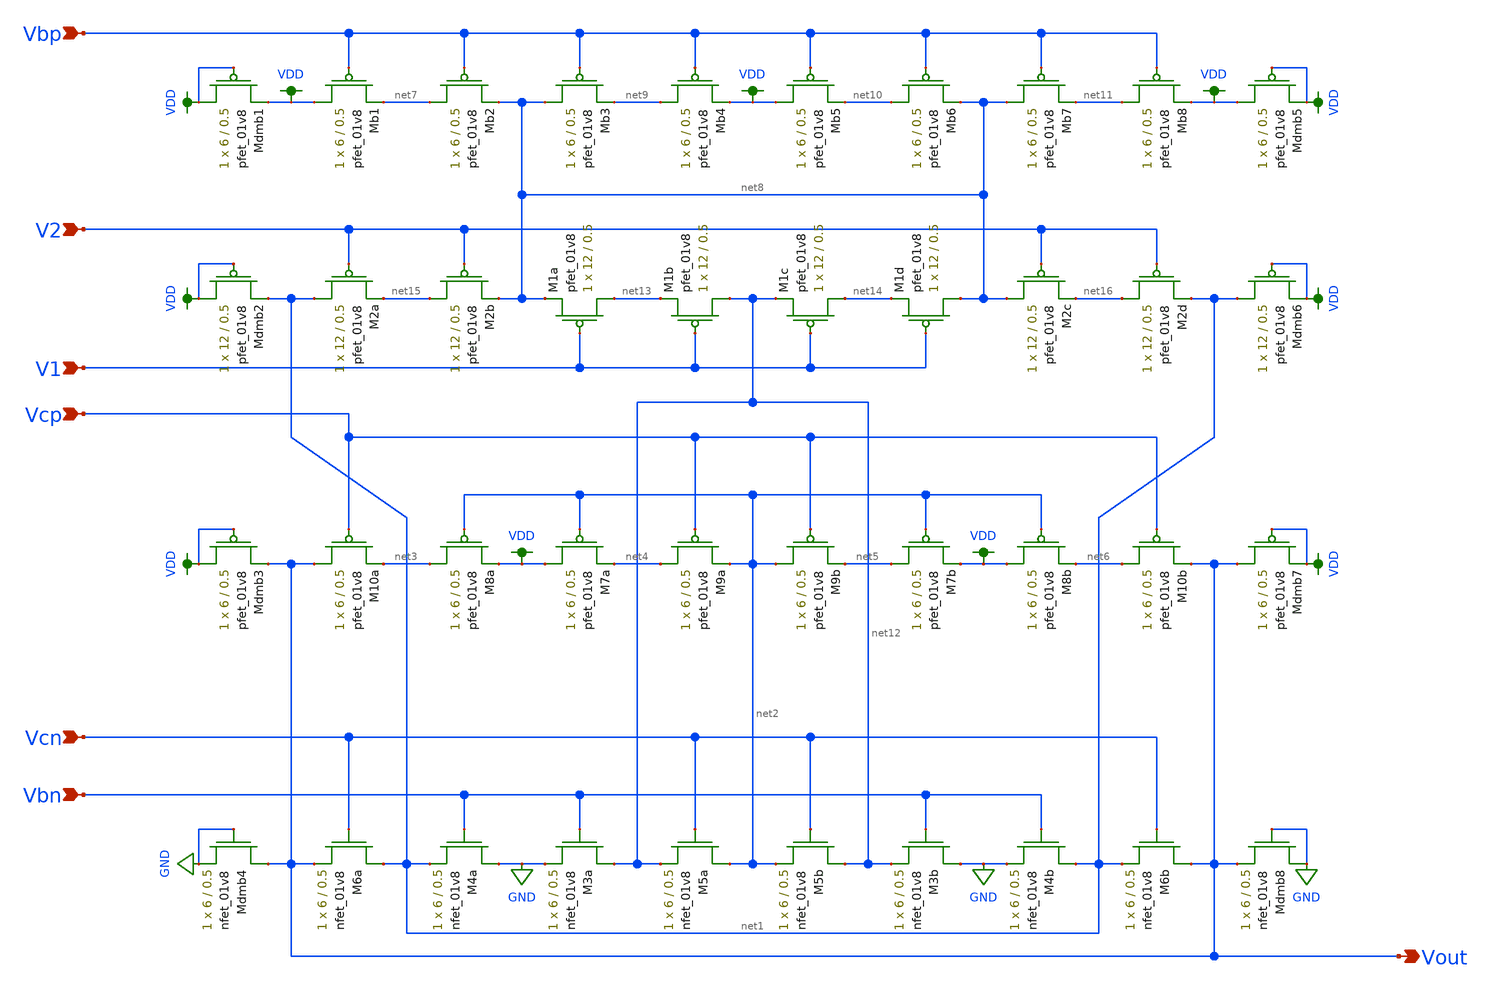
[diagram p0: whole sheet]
** sch_path: mini3/schem/cas_diff_lvs.sch
**.subckt cas_diff_lvs Vbp Vbn Vcn Vcp Vout V1 V2
*.ipin Vbp
*.ipin Vbn
*.ipin Vcn
*.ipin Vcp
*.opin Vout
*.ipin V1
*.ipin V2
XM6a net1 Vcn Vout GND sky130_fd_pr__nfet_01v8 L=0.5 W=6 nf=1 ad='int((nf+1)/2) * W/nf * 0.29' as='int((nf+2)/2) * W/nf * 0.29'
+ pd='2*int((nf+1)/2) * (W/nf + 0.29)' ps='2*int((nf+2)/2) * (W/nf + 0.29)' nrd='0.29 / W' nrs='0.29 / W'
+ sa=0 sb=0 sd=0 mult=1 m=1
XM4a GND Vbn net1 GND sky130_fd_pr__nfet_01v8 L=0.5 W=6 nf=1 ad='int((nf+1)/2) * W/nf * 0.29' as='int((nf+2)/2) * W/nf * 0.29'
+ pd='2*int((nf+1)/2) * (W/nf + 0.29)' ps='2*int((nf+2)/2) * (W/nf + 0.29)' nrd='0.29 / W' nrs='0.29 / W'
+ sa=0 sb=0 sd=0 mult=1 m=1
XM3a net12 Vbn GND GND sky130_fd_pr__nfet_01v8 L=0.5 W=6 nf=1 ad='int((nf+1)/2) * W/nf * 0.29' as='int((nf+2)/2) * W/nf * 0.29'
+ pd='2*int((nf+1)/2) * (W/nf + 0.29)' ps='2*int((nf+2)/2) * (W/nf + 0.29)' nrd='0.29 / W' nrs='0.29 / W'
+ sa=0 sb=0 sd=0 mult=1 m=1
XM5a net2 Vcn net12 GND sky130_fd_pr__nfet_01v8 L=0.5 W=6 nf=1 ad='int((nf+1)/2) * W/nf * 0.29' as='int((nf+2)/2) * W/nf * 0.29'
+ pd='2*int((nf+1)/2) * (W/nf + 0.29)' ps='2*int((nf+2)/2) * (W/nf + 0.29)' nrd='0.29 / W' nrs='0.29 / W'
+ sa=0 sb=0 sd=0 mult=1 m=1
XM5b net12 Vcn net2 GND sky130_fd_pr__nfet_01v8 L=0.5 W=6 nf=1 ad='int((nf+1)/2) * W/nf * 0.29' as='int((nf+2)/2) * W/nf * 0.29'
+ pd='2*int((nf+1)/2) * (W/nf + 0.29)' ps='2*int((nf+2)/2) * (W/nf + 0.29)' nrd='0.29 / W' nrs='0.29 / W'
+ sa=0 sb=0 sd=0 mult=1 m=1
XM3b GND Vbn net12 GND sky130_fd_pr__nfet_01v8 L=0.5 W=6 nf=1 ad='int((nf+1)/2) * W/nf * 0.29' as='int((nf+2)/2) * W/nf * 0.29'
+ pd='2*int((nf+1)/2) * (W/nf + 0.29)' ps='2*int((nf+2)/2) * (W/nf + 0.29)' nrd='0.29 / W' nrs='0.29 / W'
+ sa=0 sb=0 sd=0 mult=1 m=1
XM4b net1 Vbn GND GND sky130_fd_pr__nfet_01v8 L=0.5 W=6 nf=1 ad='int((nf+1)/2) * W/nf * 0.29' as='int((nf+2)/2) * W/nf * 0.29'
+ pd='2*int((nf+1)/2) * (W/nf + 0.29)' ps='2*int((nf+2)/2) * (W/nf + 0.29)' nrd='0.29 / W' nrs='0.29 / W'
+ sa=0 sb=0 sd=0 mult=1 m=1
XM6b Vout Vcn net1 GND sky130_fd_pr__nfet_01v8 L=0.5 W=6 nf=1 ad='int((nf+1)/2) * W/nf * 0.29' as='int((nf+2)/2) * W/nf * 0.29'
+ pd='2*int((nf+1)/2) * (W/nf + 0.29)' ps='2*int((nf+2)/2) * (W/nf + 0.29)' nrd='0.29 / W' nrs='0.29 / W'
+ sa=0 sb=0 sd=0 mult=1 m=1
XM10a Vout Vcp net3 VDD sky130_fd_pr__pfet_01v8 L=0.5 W=6 nf=1 ad='int((nf+1)/2) * W/nf * 0.29' as='int((nf+2)/2) * W/nf * 0.29'
+ pd='2*int((nf+1)/2) * (W/nf + 0.29)' ps='2*int((nf+2)/2) * (W/nf + 0.29)' nrd='0.29 / W' nrs='0.29 / W'
+ sa=0 sb=0 sd=0 mult=1 m=1
XM8a net3 net2 VDD VDD sky130_fd_pr__pfet_01v8 L=0.5 W=6 nf=1 ad='int((nf+1)/2) * W/nf * 0.29' as='int((nf+2)/2) * W/nf * 0.29'
+ pd='2*int((nf+1)/2) * (W/nf + 0.29)' ps='2*int((nf+2)/2) * (W/nf + 0.29)' nrd='0.29 / W' nrs='0.29 / W'
+ sa=0 sb=0 sd=0 mult=1 m=1
XM7a VDD net2 net4 VDD sky130_fd_pr__pfet_01v8 L=0.5 W=6 nf=1 ad='int((nf+1)/2) * W/nf * 0.29' as='int((nf+2)/2) * W/nf * 0.29'
+ pd='2*int((nf+1)/2) * (W/nf + 0.29)' ps='2*int((nf+2)/2) * (W/nf + 0.29)' nrd='0.29 / W' nrs='0.29 / W'
+ sa=0 sb=0 sd=0 mult=1 m=1
XM9a net4 Vcp net2 VDD sky130_fd_pr__pfet_01v8 L=0.5 W=6 nf=1 ad='int((nf+1)/2) * W/nf * 0.29' as='int((nf+2)/2) * W/nf * 0.29'
+ pd='2*int((nf+1)/2) * (W/nf + 0.29)' ps='2*int((nf+2)/2) * (W/nf + 0.29)' nrd='0.29 / W' nrs='0.29 / W'
+ sa=0 sb=0 sd=0 mult=1 m=1
XM9b net2 Vcp net5 VDD sky130_fd_pr__pfet_01v8 L=0.5 W=6 nf=1 ad='int((nf+1)/2) * W/nf * 0.29' as='int((nf+2)/2) * W/nf * 0.29'
+ pd='2*int((nf+1)/2) * (W/nf + 0.29)' ps='2*int((nf+2)/2) * (W/nf + 0.29)' nrd='0.29 / W' nrs='0.29 / W'
+ sa=0 sb=0 sd=0 mult=1 m=1
XM7b net5 net2 VDD VDD sky130_fd_pr__pfet_01v8 L=0.5 W=6 nf=1 ad='int((nf+1)/2) * W/nf * 0.29' as='int((nf+2)/2) * W/nf * 0.29'
+ pd='2*int((nf+1)/2) * (W/nf + 0.29)' ps='2*int((nf+2)/2) * (W/nf + 0.29)' nrd='0.29 / W' nrs='0.29 / W'
+ sa=0 sb=0 sd=0 mult=1 m=1
XM8b VDD net2 net6 VDD sky130_fd_pr__pfet_01v8 L=0.5 W=6 nf=1 ad='int((nf+1)/2) * W/nf * 0.29' as='int((nf+2)/2) * W/nf * 0.29'
+ pd='2*int((nf+1)/2) * (W/nf + 0.29)' ps='2*int((nf+2)/2) * (W/nf + 0.29)' nrd='0.29 / W' nrs='0.29 / W'
+ sa=0 sb=0 sd=0 mult=1 m=1
XM10b net6 Vcp Vout VDD sky130_fd_pr__pfet_01v8 L=0.5 W=6 nf=1 ad='int((nf+1)/2) * W/nf * 0.29' as='int((nf+2)/2) * W/nf * 0.29'
+ pd='2*int((nf+1)/2) * (W/nf + 0.29)' ps='2*int((nf+2)/2) * (W/nf + 0.29)' nrd='0.29 / W' nrs='0.29 / W'
+ sa=0 sb=0 sd=0 mult=1 m=1
XMb1 VDD Vbp net7 VDD sky130_fd_pr__pfet_01v8 L=0.5 W=6 nf=1 ad='int((nf+1)/2) * W/nf * 0.29' as='int((nf+2)/2) * W/nf * 0.29'
+ pd='2*int((nf+1)/2) * (W/nf + 0.29)' ps='2*int((nf+2)/2) * (W/nf + 0.29)' nrd='0.29 / W' nrs='0.29 / W'
+ sa=0 sb=0 sd=0 mult=1 m=1
XMb2 net7 Vbp net8 VDD sky130_fd_pr__pfet_01v8 L=0.5 W=6 nf=1 ad='int((nf+1)/2) * W/nf * 0.29' as='int((nf+2)/2) * W/nf * 0.29'
+ pd='2*int((nf+1)/2) * (W/nf + 0.29)' ps='2*int((nf+2)/2) * (W/nf + 0.29)' nrd='0.29 / W' nrs='0.29 / W'
+ sa=0 sb=0 sd=0 mult=1 m=1
XMb3 net8 Vbp net9 VDD sky130_fd_pr__pfet_01v8 L=0.5 W=6 nf=1 ad='int((nf+1)/2) * W/nf * 0.29' as='int((nf+2)/2) * W/nf * 0.29'
+ pd='2*int((nf+1)/2) * (W/nf + 0.29)' ps='2*int((nf+2)/2) * (W/nf + 0.29)' nrd='0.29 / W' nrs='0.29 / W'
+ sa=0 sb=0 sd=0 mult=1 m=1
XMb4 net9 Vbp VDD VDD sky130_fd_pr__pfet_01v8 L=0.5 W=6 nf=1 ad='int((nf+1)/2) * W/nf * 0.29' as='int((nf+2)/2) * W/nf * 0.29'
+ pd='2*int((nf+1)/2) * (W/nf + 0.29)' ps='2*int((nf+2)/2) * (W/nf + 0.29)' nrd='0.29 / W' nrs='0.29 / W'
+ sa=0 sb=0 sd=0 mult=1 m=1
XMb5 VDD Vbp net10 VDD sky130_fd_pr__pfet_01v8 L=0.5 W=6 nf=1 ad='int((nf+1)/2) * W/nf * 0.29' as='int((nf+2)/2) * W/nf * 0.29'
+ pd='2*int((nf+1)/2) * (W/nf + 0.29)' ps='2*int((nf+2)/2) * (W/nf + 0.29)' nrd='0.29 / W' nrs='0.29 / W'
+ sa=0 sb=0 sd=0 mult=1 m=1
XMb6 net10 Vbp net8 VDD sky130_fd_pr__pfet_01v8 L=0.5 W=6 nf=1 ad='int((nf+1)/2) * W/nf * 0.29' as='int((nf+2)/2) * W/nf * 0.29'
+ pd='2*int((nf+1)/2) * (W/nf + 0.29)' ps='2*int((nf+2)/2) * (W/nf + 0.29)' nrd='0.29 / W' nrs='0.29 / W'
+ sa=0 sb=0 sd=0 mult=1 m=1
XMb7 net8 Vbp net11 VDD sky130_fd_pr__pfet_01v8 L=0.5 W=6 nf=1 ad='int((nf+1)/2) * W/nf * 0.29' as='int((nf+2)/2) * W/nf * 0.29'
+ pd='2*int((nf+1)/2) * (W/nf + 0.29)' ps='2*int((nf+2)/2) * (W/nf + 0.29)' nrd='0.29 / W' nrs='0.29 / W'
+ sa=0 sb=0 sd=0 mult=1 m=1
XMb8 net11 Vbp VDD VDD sky130_fd_pr__pfet_01v8 L=0.5 W=6 nf=1 ad='int((nf+1)/2) * W/nf * 0.29' as='int((nf+2)/2) * W/nf * 0.29'
+ pd='2*int((nf+1)/2) * (W/nf + 0.29)' ps='2*int((nf+2)/2) * (W/nf + 0.29)' nrd='0.29 / W' nrs='0.29 / W'
+ sa=0 sb=0 sd=0 mult=1 m=1
XM1a net13 V1 net8 VDD sky130_fd_pr__pfet_01v8 L=0.5 W=12 nf=1 ad='int((nf+1)/2) * W/nf * 0.29' as='int((nf+2)/2) * W/nf * 0.29'
+ pd='2*int((nf+1)/2) * (W/nf + 0.29)' ps='2*int((nf+2)/2) * (W/nf + 0.29)' nrd='0.29 / W' nrs='0.29 / W'
+ sa=0 sb=0 sd=0 mult=1 m=1
XM1b net12 V1 net13 VDD sky130_fd_pr__pfet_01v8 L=0.5 W=12 nf=1 ad='int((nf+1)/2) * W/nf * 0.29' as='int((nf+2)/2) * W/nf * 0.29'
+ pd='2*int((nf+1)/2) * (W/nf + 0.29)' ps='2*int((nf+2)/2) * (W/nf + 0.29)' nrd='0.29 / W' nrs='0.29 / W'
+ sa=0 sb=0 sd=0 mult=1 m=1
XM2a net1 V2 net15 VDD sky130_fd_pr__pfet_01v8 L=0.5 W=12 nf=1 ad='int((nf+1)/2) * W/nf * 0.29' as='int((nf+2)/2) * W/nf * 0.29'
+ pd='2*int((nf+1)/2) * (W/nf + 0.29)' ps='2*int((nf+2)/2) * (W/nf + 0.29)' nrd='0.29 / W' nrs='0.29 / W'
+ sa=0 sb=0 sd=0 mult=1 m=1
XM2b net15 V2 net8 VDD sky130_fd_pr__pfet_01v8 L=0.5 W=12 nf=1 ad='int((nf+1)/2) * W/nf * 0.29' as='int((nf+2)/2) * W/nf * 0.29'
+ pd='2*int((nf+1)/2) * (W/nf + 0.29)' ps='2*int((nf+2)/2) * (W/nf + 0.29)' nrd='0.29 / W' nrs='0.29 / W'
+ sa=0 sb=0 sd=0 mult=1 m=1
XM2c net8 V2 net16 VDD sky130_fd_pr__pfet_01v8 L=0.5 W=12 nf=1 ad='int((nf+1)/2) * W/nf * 0.29' as='int((nf+2)/2) * W/nf * 0.29'
+ pd='2*int((nf+1)/2) * (W/nf + 0.29)' ps='2*int((nf+2)/2) * (W/nf + 0.29)' nrd='0.29 / W' nrs='0.29 / W'
+ sa=0 sb=0 sd=0 mult=1 m=1
XM2d net16 V2 net1 VDD sky130_fd_pr__pfet_01v8 L=0.5 W=12 nf=1 ad='int((nf+1)/2) * W/nf * 0.29' as='int((nf+2)/2) * W/nf * 0.29'
+ pd='2*int((nf+1)/2) * (W/nf + 0.29)' ps='2*int((nf+2)/2) * (W/nf + 0.29)' nrd='0.29 / W' nrs='0.29 / W'
+ sa=0 sb=0 sd=0 mult=1 m=1
XM1c net14 V1 net12 VDD sky130_fd_pr__pfet_01v8 L=0.5 W=12 nf=1 ad='int((nf+1)/2) * W/nf * 0.29' as='int((nf+2)/2) * W/nf * 0.29'
+ pd='2*int((nf+1)/2) * (W/nf + 0.29)' ps='2*int((nf+2)/2) * (W/nf + 0.29)' nrd='0.29 / W' nrs='0.29 / W'
+ sa=0 sb=0 sd=0 mult=1 m=1
XM1d net8 V1 net14 VDD sky130_fd_pr__pfet_01v8 L=0.5 W=12 nf=1 ad='int((nf+1)/2) * W/nf * 0.29' as='int((nf+2)/2) * W/nf * 0.29'
+ pd='2*int((nf+1)/2) * (W/nf + 0.29)' ps='2*int((nf+2)/2) * (W/nf + 0.29)' nrd='0.29 / W' nrs='0.29 / W'
+ sa=0 sb=0 sd=0 mult=1 m=1
XMdmb3 VDD VDD Vout VDD sky130_fd_pr__pfet_01v8 L=0.5 W=6 nf=1 ad='int((nf+1)/2) * W/nf * 0.29' as='int((nf+2)/2) * W/nf * 0.29'
+ pd='2*int((nf+1)/2) * (W/nf + 0.29)' ps='2*int((nf+2)/2) * (W/nf + 0.29)' nrd='0.29 / W' nrs='0.29 / W'
+ sa=0 sb=0 sd=0 mult=1 m=1
XMdmb2 VDD VDD net1 VDD sky130_fd_pr__pfet_01v8 L=0.5 W=12 nf=1 ad='int((nf+1)/2) * W/nf * 0.29' as='int((nf+2)/2) * W/nf * 0.29'
+ pd='2*int((nf+1)/2) * (W/nf + 0.29)' ps='2*int((nf+2)/2) * (W/nf + 0.29)' nrd='0.29 / W' nrs='0.29 / W'
+ sa=0 sb=0 sd=0 mult=1 m=1
XMdmb1 VDD VDD VDD VDD sky130_fd_pr__pfet_01v8 L=0.5 W=6 nf=1 ad='int((nf+1)/2) * W/nf * 0.29' as='int((nf+2)/2) * W/nf * 0.29'
+ pd='2*int((nf+1)/2) * (W/nf + 0.29)' ps='2*int((nf+2)/2) * (W/nf + 0.29)' nrd='0.29 / W' nrs='0.29 / W'
+ sa=0 sb=0 sd=0 mult=1 m=1
XMdmb7 Vout VDD VDD VDD sky130_fd_pr__pfet_01v8 L=0.5 W=6 nf=1 ad='int((nf+1)/2) * W/nf * 0.29' as='int((nf+2)/2) * W/nf * 0.29'
+ pd='2*int((nf+1)/2) * (W/nf + 0.29)' ps='2*int((nf+2)/2) * (W/nf + 0.29)' nrd='0.29 / W' nrs='0.29 / W'
+ sa=0 sb=0 sd=0 mult=1 m=1
XMdmb6 net1 VDD VDD VDD sky130_fd_pr__pfet_01v8 L=0.5 W=12 nf=1 ad='int((nf+1)/2) * W/nf * 0.29' as='int((nf+2)/2) * W/nf * 0.29'
+ pd='2*int((nf+1)/2) * (W/nf + 0.29)' ps='2*int((nf+2)/2) * (W/nf + 0.29)' nrd='0.29 / W' nrs='0.29 / W'
+ sa=0 sb=0 sd=0 mult=1 m=1
XMdmb5 VDD VDD VDD VDD sky130_fd_pr__pfet_01v8 L=0.5 W=6 nf=1 ad='int((nf+1)/2) * W/nf * 0.29' as='int((nf+2)/2) * W/nf * 0.29'
+ pd='2*int((nf+1)/2) * (W/nf + 0.29)' ps='2*int((nf+2)/2) * (W/nf + 0.29)' nrd='0.29 / W' nrs='0.29 / W'
+ sa=0 sb=0 sd=0 mult=1 m=1
XMdmb4 Vout GND GND GND sky130_fd_pr__nfet_01v8 L=0.5 W=6 nf=1 ad='int((nf+1)/2) * W/nf * 0.29' as='int((nf+2)/2) * W/nf * 0.29'
+ pd='2*int((nf+1)/2) * (W/nf + 0.29)' ps='2*int((nf+2)/2) * (W/nf + 0.29)' nrd='0.29 / W' nrs='0.29 / W'
+ sa=0 sb=0 sd=0 mult=1 m=1
XMdmb8 GND GND Vout GND sky130_fd_pr__nfet_01v8 L=0.5 W=6 nf=1 ad='int((nf+1)/2) * W/nf * 0.29' as='int((nf+2)/2) * W/nf * 0.29'
+ pd='2*int((nf+1)/2) * (W/nf + 0.29)' ps='2*int((nf+2)/2) * (W/nf + 0.29)' nrd='0.29 / W' nrs='0.29 / W'
+ sa=0 sb=0 sd=0 mult=1 m=1
**.ends
.GLOBAL VDD
.GLOBAL GND
.end
